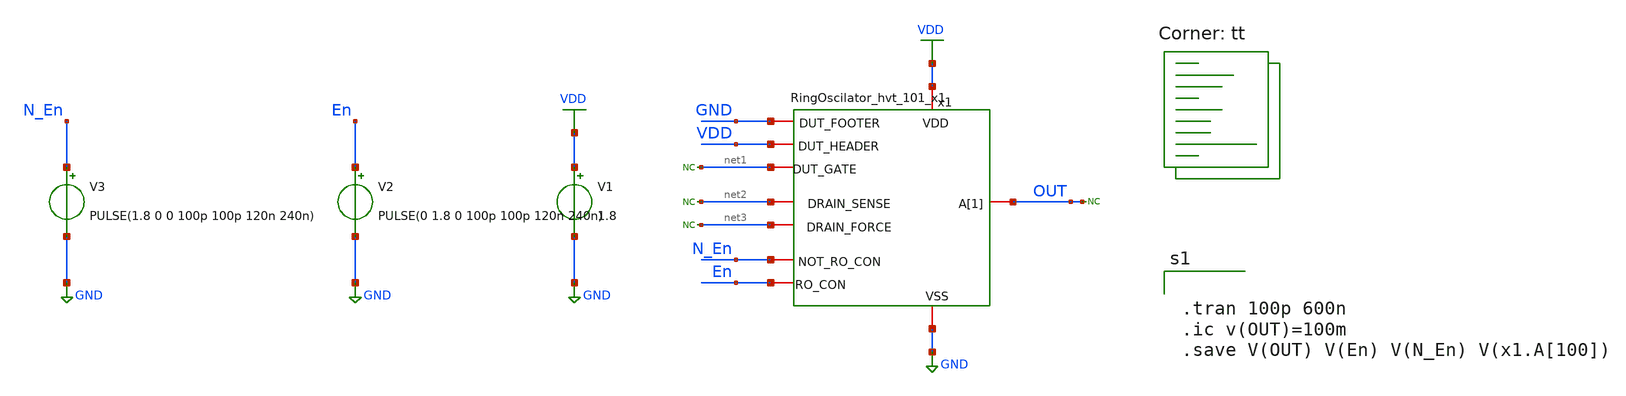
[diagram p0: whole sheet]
** sch_path: HVT/tb_RingOscilator_hvt_101/tb_RingOscilator_hvt_101.sch
**.subckt tb_RingOscilator_hvt_101
V1 VDD GND 1.8
* noconn #net1
* noconn #net2
* noconn #net3
* noconn OUT
V2 En GND PULSE(0 1.8 0 100p 100p 120n 240n)
V3 N_En GND PULSE(1.8 0 0 100p 100p 120n 240n)
x1 GND VDD VDD GND net1 N_En En net2 OUT net3 RingOscilator_hvt_101_x1
**** begin user architecture code
.lib $::SKYWATER_MODELS/sky130.lib.spice tt


.tran 100p 600n
.ic v(OUT)=100m
.save V(OUT) V(En) V(N_En) V(x1.A[100])


**** end user architecture code
**.ends

* expanding   symbol:
*+  /foss/designs/RO_Aging_UNICASS/HVT/RingOscilator_hvt_101_x1/RingOscilator_hvt_101_x1.sym # of pins=10
** sym_path: HVT/RingOscilator_hvt_101_x1/RingOscilator_hvt_101_x1.sym
** sch_path: HVT/RingOscilator_hvt_101_x1/RingOscilator_hvt_101_x1.sch
.subckt RingOscilator_hvt_101_x1 DUT_FOOTER VDD DUT_HEADER VSS DUT_GATE NOT_RO_CON RO_CON
+ DRAIN_SENSE A[1] DRAIN_FORCE
*.iopin VDD
*.iopin VSS
*.iopin NOT_RO_CON
*.iopin RO_CON
*.iopin DUT_FOOTER
*.iopin DUT_HEADER
*.iopin DUT_GATE
*.iopin DRAIN_SENSE
*.iopin DRAIN_FORCE
*.iopin A[1]
XM3 A[99] A[98] net1 VDD sky130_fd_pr__pfet_01v8_hvt L=0.15 W=19 nf=1 ad='int((nf+1)/2) * W/nf * 0.29'
+ as='int((nf+2)/2) * W/nf * 0.29' pd='2*int((nf+1)/2) * (W/nf + 0.29)' ps='2*int((nf+2)/2) * (W/nf + 0.29)'
+ nrd='0.29 / W' nrs='0.29 / W' sa=0 sb=0 sd=0 mult=1 m=1
XM4 net1 NOT_RO_CON VDD VDD sky130_fd_pr__pfet_01v8_hvt L=0.15 W=19 nf=1 ad='int((nf+1)/2) * W/nf * 0.29'
+ as='int((nf+2)/2) * W/nf * 0.29' pd='2*int((nf+1)/2) * (W/nf + 0.29)' ps='2*int((nf+2)/2) * (W/nf + 0.29)'
+ nrd='0.29 / W' nrs='0.29 / W' sa=0 sb=0 sd=0 mult=10 m=10
XM7 A[100] A[99] net4 VDD sky130_fd_pr__pfet_01v8_hvt L=0.15 W=19 nf=1 ad='int((nf+1)/2) * W/nf * 0.29'
+ as='int((nf+2)/2) * W/nf * 0.29' pd='2*int((nf+1)/2) * (W/nf + 0.29)' ps='2*int((nf+2)/2) * (W/nf + 0.29)'
+ nrd='0.29 / W' nrs='0.29 / W' sa=0 sb=0 sd=0 mult=1 m=1
XM8 net4 DUT_FOOTER VDD VDD sky130_fd_pr__pfet_01v8_hvt L=0.15 W=19 nf=1 ad='int((nf+1)/2) * W/nf * 0.29'
+ as='int((nf+2)/2) * W/nf * 0.29' pd='2*int((nf+1)/2) * (W/nf + 0.29)' ps='2*int((nf+2)/2) * (W/nf + 0.29)'
+ nrd='0.29 / W' nrs='0.29 / W' sa=0 sb=0 sd=0 mult=10 m=10
XM10 A[101] A[100] net6 VDD sky130_fd_pr__pfet_01v8_hvt L=0.15 W=19 nf=1 ad='int((nf+1)/2) * W/nf * 0.29'
+ as='int((nf+2)/2) * W/nf * 0.29' pd='2*int((nf+1)/2) * (W/nf + 0.29)' ps='2*int((nf+2)/2) * (W/nf + 0.29)'
+ nrd='0.29 / W' nrs='0.29 / W' sa=0 sb=0 sd=0 mult=1 m=1
XM11 net6 NOT_RO_CON VDD VDD sky130_fd_pr__pfet_01v8_hvt L=0.15 W=19 nf=1 ad='int((nf+1)/2) * W/nf * 0.29'
+ as='int((nf+2)/2) * W/nf * 0.29' pd='2*int((nf+1)/2) * (W/nf + 0.29)' ps='2*int((nf+2)/2) * (W/nf + 0.29)'
+ nrd='0.29 / W' nrs='0.29 / W' sa=0 sb=0 sd=0 mult=10 m=10
XM1 A[99] A[98] net2 VSS sky130_fd_pr__nfet_01v8 L=0.15 W=4.2 nf=1 ad='int((nf+1)/2) * W/nf * 0.29' as='int((nf+2)/2) * W/nf * 0.29'
+ pd='2*int((nf+1)/2) * (W/nf + 0.29)' ps='2*int((nf+2)/2) * (W/nf + 0.29)' nrd='0.29 / W' nrs='0.29 / W'
+ sa=0 sb=0 sd=0 mult=1 m=1
XM2 net2 RO_CON VSS VSS sky130_fd_pr__nfet_01v8 L=0.15 W=42 nf=1 ad='int((nf+1)/2) * W/nf * 0.29' as='int((nf+2)/2) * W/nf * 0.29'
+ pd='2*int((nf+1)/2) * (W/nf + 0.29)' ps='2*int((nf+2)/2) * (W/nf + 0.29)' nrd='0.29 / W' nrs='0.29 / W'
+ sa=0 sb=0 sd=0 mult=1 m=1
XM5 A[100] A[99] net5 VSS sky130_fd_pr__nfet_01v8 L=0.15 W=4.2 nf=1 ad='int((nf+1)/2) * W/nf * 0.29'
+ as='int((nf+2)/2) * W/nf * 0.29' pd='2*int((nf+1)/2) * (W/nf + 0.29)' ps='2*int((nf+2)/2) * (W/nf + 0.29)'
+ nrd='0.29 / W' nrs='0.29 / W' sa=0 sb=0 sd=0 mult=1 m=1
XM6 net5 DUT_HEADER VSS VSS sky130_fd_pr__nfet_01v8 L=0.15 W=42 nf=1 ad='int((nf+1)/2) * W/nf * 0.29'
+ as='int((nf+2)/2) * W/nf * 0.29' pd='2*int((nf+1)/2) * (W/nf + 0.29)' ps='2*int((nf+2)/2) * (W/nf + 0.29)'
+ nrd='0.29 / W' nrs='0.29 / W' sa=0 sb=0 sd=0 mult=1 m=1
XM9 A[101] A[100] VSS VSS sky130_fd_pr__nfet_01v8 L=0.15 W=4.2 nf=1 ad='int((nf+1)/2) * W/nf * 0.29'
+ as='int((nf+2)/2) * W/nf * 0.29' pd='2*int((nf+1)/2) * (W/nf + 0.29)' ps='2*int((nf+2)/2) * (W/nf + 0.29)'
+ nrd='0.29 / W' nrs='0.29 / W' sa=0 sb=0 sd=0 mult=1 m=1
x4[1] VDD VSS A[1] A[2] RingStage
x4[2] VDD VSS A[2] A[3] RingStage
x4[3] VDD VSS A[3] A[4] RingStage
x4[4] VDD VSS A[4] A[5] RingStage
x4[5] VDD VSS A[5] A[6] RingStage
x4[6] VDD VSS A[6] A[7] RingStage
x4[7] VDD VSS A[7] A[8] RingStage
x4[8] VDD VSS A[8] A[9] RingStage
x4[9] VDD VSS A[9] A[10] RingStage
x4[10] VDD VSS A[10] A[11] RingStage
x4[11] VDD VSS A[11] A[12] RingStage
x4[12] VDD VSS A[12] A[13] RingStage
x4[13] VDD VSS A[13] A[14] RingStage
x4[14] VDD VSS A[14] A[15] RingStage
x4[15] VDD VSS A[15] A[16] RingStage
x4[16] VDD VSS A[16] A[17] RingStage
x4[17] VDD VSS A[17] A[18] RingStage
x4[18] VDD VSS A[18] A[19] RingStage
x4[19] VDD VSS A[19] A[20] RingStage
x4[20] VDD VSS A[20] A[21] RingStage
x4[21] VDD VSS A[21] A[22] RingStage
x4[22] VDD VSS A[22] A[23] RingStage
x4[23] VDD VSS A[23] A[24] RingStage
x4[24] VDD VSS A[24] A[25] RingStage
x4[25] VDD VSS A[25] A[26] RingStage
x4[26] VDD VSS A[26] A[27] RingStage
x4[27] VDD VSS A[27] A[28] RingStage
x4[28] VDD VSS A[28] A[29] RingStage
x4[29] VDD VSS A[29] A[30] RingStage
x4[30] VDD VSS A[30] A[31] RingStage
x4[31] VDD VSS A[31] A[32] RingStage
x4[32] VDD VSS A[32] A[33] RingStage
x4[33] VDD VSS A[33] A[34] RingStage
x4[34] VDD VSS A[34] A[35] RingStage
x4[35] VDD VSS A[35] A[36] RingStage
x4[36] VDD VSS A[36] A[37] RingStage
x4[37] VDD VSS A[37] A[38] RingStage
x4[38] VDD VSS A[38] A[39] RingStage
x4[39] VDD VSS A[39] A[40] RingStage
x4[40] VDD VSS A[40] A[41] RingStage
x4[41] VDD VSS A[41] A[42] RingStage
x4[42] VDD VSS A[42] A[43] RingStage
x4[43] VDD VSS A[43] A[44] RingStage
x4[44] VDD VSS A[44] A[45] RingStage
x4[45] VDD VSS A[45] A[46] RingStage
x4[46] VDD VSS A[46] A[47] RingStage
x4[47] VDD VSS A[47] A[48] RingStage
x4[48] VDD VSS A[48] A[49] RingStage
x4[49] VDD VSS A[49] A[50] RingStage
x4[50] VDD VSS A[50] A[51] RingStage
x4[51] VDD VSS A[51] A[52] RingStage
x4[52] VDD VSS A[52] A[53] RingStage
x4[53] VDD VSS A[53] A[54] RingStage
x4[54] VDD VSS A[54] A[55] RingStage
x4[55] VDD VSS A[55] A[56] RingStage
x4[56] VDD VSS A[56] A[57] RingStage
x4[57] VDD VSS A[57] A[58] RingStage
x4[58] VDD VSS A[58] A[59] RingStage
x4[59] VDD VSS A[59] A[60] RingStage
x4[60] VDD VSS A[60] A[61] RingStage
x4[61] VDD VSS A[61] A[62] RingStage
x4[62] VDD VSS A[62] A[63] RingStage
x4[63] VDD VSS A[63] A[64] RingStage
x4[64] VDD VSS A[64] A[65] RingStage
x4[65] VDD VSS A[65] A[66] RingStage
x4[66] VDD VSS A[66] A[67] RingStage
x4[67] VDD VSS A[67] A[68] RingStage
x4[68] VDD VSS A[68] A[69] RingStage
x4[69] VDD VSS A[69] A[70] RingStage
x4[70] VDD VSS A[70] A[71] RingStage
x4[71] VDD VSS A[71] A[72] RingStage
x4[72] VDD VSS A[72] A[73] RingStage
x4[73] VDD VSS A[73] A[74] RingStage
x4[74] VDD VSS A[74] A[75] RingStage
x4[75] VDD VSS A[75] A[76] RingStage
x4[76] VDD VSS A[76] A[77] RingStage
x4[77] VDD VSS A[77] A[78] RingStage
x4[78] VDD VSS A[78] A[79] RingStage
x4[79] VDD VSS A[79] A[80] RingStage
x4[80] VDD VSS A[80] A[81] RingStage
x4[81] VDD VSS A[81] A[82] RingStage
x4[82] VDD VSS A[82] A[83] RingStage
x4[83] VDD VSS A[83] A[84] RingStage
x4[84] VDD VSS A[84] A[85] RingStage
x4[85] VDD VSS A[85] A[86] RingStage
x4[86] VDD VSS A[86] A[87] RingStage
x4[87] VDD VSS A[87] A[88] RingStage
x4[88] VDD VSS A[88] A[89] RingStage
x4[89] VDD VSS A[89] A[90] RingStage
x4[90] VDD VSS A[90] A[91] RingStage
x4[91] VDD VSS A[91] A[92] RingStage
x4[92] VDD VSS A[92] A[93] RingStage
x4[93] VDD VSS A[93] A[94] RingStage
x4[94] VDD VSS A[94] A[95] RingStage
x4[95] VDD VSS A[95] A[96] RingStage
x4[96] VDD VSS A[96] A[97] RingStage
x4[97] VDD VSS A[97] A[98] RingStage
x1 A[99] RO_CON VSS VDD NOT_RO_CON net3 passGate_hvt
x4 A[99] RO_CON VSS VDD NOT_RO_CON DUT_GATE passGate_hvt
x6 A[101] VDD VSS VDD NOT_RO_CON VSS passGate_hvt
x7 A[101] VDD VSS VDD NOT_RO_CON net7 passGate_hvt
x3 VDD VSS A[101] A[1] RingStage
XM12 A[100] RO_CON DRAIN_SENSE VDD sky130_fd_pr__pfet_01v8_hvt L=0.15 W=19 nf=1 ad='int((nf+1)/2) * W/nf * 0.29'
+ as='int((nf+2)/2) * W/nf * 0.29' pd='2*int((nf+1)/2) * (W/nf + 0.29)' ps='2*int((nf+2)/2) * (W/nf + 0.29)'
+ nrd='0.29 / W' nrs='0.29 / W' sa=0 sb=0 sd=0 mult=1 m=1
XM13 A[100] NOT_RO_CON DRAIN_SENSE VSS sky130_fd_pr__nfet_01v8 L=0.15 W=4.2 nf=1 ad='int((nf+1)/2) * W/nf * 0.29'
+ as='int((nf+2)/2) * W/nf * 0.29' pd='2*int((nf+1)/2) * (W/nf + 0.29)' ps='2*int((nf+2)/2) * (W/nf + 0.29)'
+ nrd='0.29 / W' nrs='0.29 / W' sa=0 sb=0 sd=0 mult=1 m=1
XM14 A[100] RO_CON DRAIN_FORCE VDD sky130_fd_pr__pfet_01v8_hvt L=0.15 W=19 nf=1 ad='int((nf+1)/2) * W/nf * 0.29'
+ as='int((nf+2)/2) * W/nf * 0.29' pd='2*int((nf+1)/2) * (W/nf + 0.29)' ps='2*int((nf+2)/2) * (W/nf + 0.29)'
+ nrd='0.29 / W' nrs='0.29 / W' sa=0 sb=0 sd=0 mult=1 m=1
XM15 A[100] NOT_RO_CON DRAIN_FORCE VSS sky130_fd_pr__nfet_01v8 L=0.15 W=4.2 nf=1 ad='int((nf+1)/2) * W/nf * 0.29'
+ as='int((nf+2)/2) * W/nf * 0.29' pd='2*int((nf+1)/2) * (W/nf + 0.29)' ps='2*int((nf+2)/2) * (W/nf + 0.29)'
+ nrd='0.29 / W' nrs='0.29 / W' sa=0 sb=0 sd=0 mult=1 m=1
.ends


* expanding   symbol:  /foss/designs/RO_Aging_UNICASS/HVT/RingStage/RingStage.sym # of pins=4
** sym_path: HVT/RingStage/RingStage.sym
** sch_path: HVT/RingStage/RingStage.sch
.subckt RingStage VDD VSS In Out
*.iopin In
*.iopin Out
*.iopin VDD
*.iopin VSS
XM2 Out In VDD VDD sky130_fd_pr__pfet_01v8_hvt L=0.15 W=4.75 nf=1 ad='int((nf+1)/2) * W/nf * 0.29' as='int((nf+2)/2) * W/nf * 0.29'
+ pd='2*int((nf+1)/2) * (W/nf + 0.29)' ps='2*int((nf+2)/2) * (W/nf + 0.29)' nrd='0.29 / W' nrs='0.29 / W'
+ sa=0 sb=0 sd=0 mult=4 m=4
XM1 Out In VSS VSS sky130_fd_pr__nfet_01v8 L=0.15 W=2.1 nf=1 ad='int((nf+1)/2) * W/nf * 0.29' as='int((nf+2)/2) * W/nf * 0.29'
+ pd='2*int((nf+1)/2) * (W/nf + 0.29)' ps='2*int((nf+2)/2) * (W/nf + 0.29)' nrd='0.29 / W' nrs='0.29 / W'
+ sa=0 sb=0 sd=0 mult=2 m=2
XM3 Out VDD net1 VDD sky130_fd_pr__pfet_01v8_hvt L=0.15 W=0.45 nf=1 ad='int((nf+1)/2) * W/nf * 0.29'
+ as='int((nf+2)/2) * W/nf * 0.29' pd='2*int((nf+1)/2) * (W/nf + 0.29)' ps='2*int((nf+2)/2) * (W/nf + 0.29)'
+ nrd='0.29 / W' nrs='0.29 / W' sa=0 sb=0 sd=0 mult=1 m=1
XM4 Out VSS net1 VSS sky130_fd_pr__nfet_01v8 L=0.15 W=0.45 nf=1 ad='int((nf+1)/2) * W/nf * 0.29' as='int((nf+2)/2) * W/nf * 0.29'
+ pd='2*int((nf+1)/2) * (W/nf + 0.29)' ps='2*int((nf+2)/2) * (W/nf + 0.29)' nrd='0.29 / W' nrs='0.29 / W'
+ sa=0 sb=0 sd=0 mult=1 m=1
XM5 Out VDD net2 VDD sky130_fd_pr__pfet_01v8_hvt L=0.15 W=0.45 nf=1 ad='int((nf+1)/2) * W/nf * 0.29'
+ as='int((nf+2)/2) * W/nf * 0.29' pd='2*int((nf+1)/2) * (W/nf + 0.29)' ps='2*int((nf+2)/2) * (W/nf + 0.29)'
+ nrd='0.29 / W' nrs='0.29 / W' sa=0 sb=0 sd=0 mult=1 m=1
XM6 Out VSS net2 VSS sky130_fd_pr__nfet_01v8 L=0.15 W=0.45 nf=1 ad='int((nf+1)/2) * W/nf * 0.29' as='int((nf+2)/2) * W/nf * 0.29'
+ pd='2*int((nf+1)/2) * (W/nf + 0.29)' ps='2*int((nf+2)/2) * (W/nf + 0.29)' nrd='0.29 / W' nrs='0.29 / W'
+ sa=0 sb=0 sd=0 mult=1 m=1
* noconn #net1
* noconn #net2
.ends


* expanding   symbol:  /foss/designs/RO_Aging_UNICASS/HVT/passGate_hvt/passGate_hvt.sym # of pins=6
** sym_path: HVT/passGate_hvt/passGate_hvt.sym
** sch_path: HVT/passGate_hvt/passGate_hvt.sch
.subckt passGate_hvt In CLKN VSS VDD CLK Out
*.iopin In
*.iopin CLKN
*.iopin Out
*.iopin VSS
*.iopin VDD
*.iopin CLK
XM2 Out CLKN In VDD sky130_fd_pr__pfet_01v8_hvt L=0.15 W=0.45 nf=1 ad='int((nf+1)/2) * W/nf * 0.29' as='int((nf+2)/2) * W/nf * 0.29'
+ pd='2*int((nf+1)/2) * (W/nf + 0.29)' ps='2*int((nf+2)/2) * (W/nf + 0.29)' nrd='0.29 / W' nrs='0.29 / W'
+ sa=0 sb=0 sd=0 mult=1 m=1
XM1 Out CLK In VSS sky130_fd_pr__nfet_01v8 L=0.15 W=0.45 nf=1 ad='int((nf+1)/2) * W/nf * 0.29' as='int((nf+2)/2) * W/nf * 0.29'
+ pd='2*int((nf+1)/2) * (W/nf + 0.29)' ps='2*int((nf+2)/2) * (W/nf + 0.29)' nrd='0.29 / W' nrs='0.29 / W'
+ sa=0 sb=0 sd=0 mult=1 m=1
.ends

.GLOBAL VDD
.GLOBAL GND
.end
